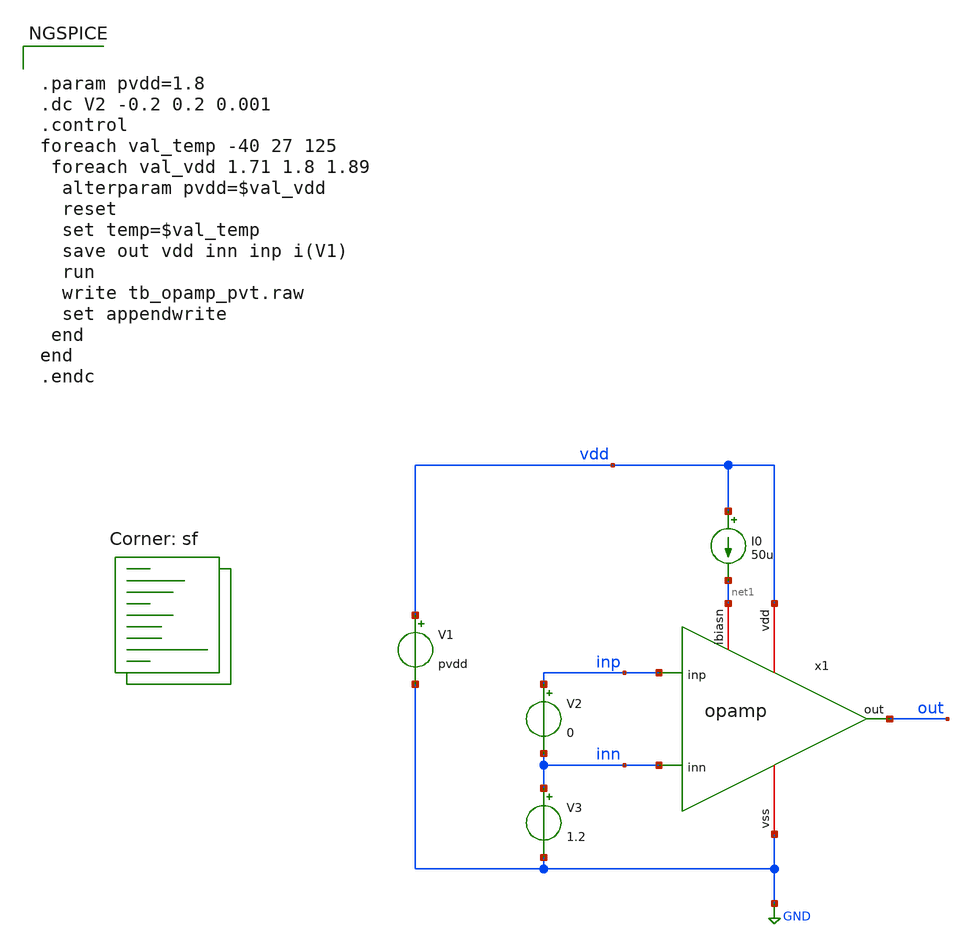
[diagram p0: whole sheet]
** sch_path: sky130A/HelloWorld/analog/schematic/tb_opamp_pvt.sch
**.subckt tb_opamp_pvt
x1 vdd out inp inn net1 GND opamp
V1 vdd GND pvdd
I0 vdd net1 50u
V2 inp inn 0
V3 inn GND 1.2
**** begin user architecture code


.param pvdd=1.8
.dc V2 -0.2 0.2 0.001
.control
foreach val_temp -40 27 125
 foreach val_vdd 1.71 1.8 1.89
  alterparam pvdd=$val_vdd
  reset
  set temp=$val_temp
  save out vdd inn inp i(V1)
  run
  write tb_opamp_pvt.raw
  set appendwrite
 end
end
.endc


.lib $::SKYWATER_MODELS/sky130.lib.spice sf
**** end user architecture code
**.ends

* expanding   symbol:  opamp.sym # of pins=6
** sym_path: sky130A/HelloWorld/xschem/opamp.sym
** sch_path: sky130A/HelloWorld/xschem/opamp.sch
.subckt opamp vdd out inp inn ibiasn vss
*.ipin inn
*.ipin inp
*.iopin vdd
*.iopin vss
*.iopin ibiasn
*.opin out
XM1 pbias inn tail vss sky130_fd_pr__nfet_01v8 L=1 W=40 nf=1 ad='int((nf+1)/2) * W/nf * 0.29' as='int((nf+2)/2) * W/nf * 0.29'
+ pd='2*int((nf+1)/2) * (W/nf + 0.29)' ps='2*int((nf+2)/2) * (W/nf + 0.29)' nrd='0.29 / W' nrs='0.29 / W'
+ sa=0 sb=0 sd=0 mult=1 m=1
XM2 outz inp tail vss sky130_fd_pr__nfet_01v8 L=1 W=40 nf=1 ad='int((nf+1)/2) * W/nf * 0.29' as='int((nf+2)/2) * W/nf * 0.29'
+ pd='2*int((nf+1)/2) * (W/nf + 0.29)' ps='2*int((nf+2)/2) * (W/nf + 0.29)' nrd='0.29 / W' nrs='0.29 / W'
+ sa=0 sb=0 sd=0 mult=1 m=1
XM3 pbias pbias vdd vdd sky130_fd_pr__pfet_01v8 L=0.5 W=20 nf=1 ad='int((nf+1)/2) * W/nf * 0.29' as='int((nf+2)/2) * W/nf * 0.29'
+ pd='2*int((nf+1)/2) * (W/nf + 0.29)' ps='2*int((nf+2)/2) * (W/nf + 0.29)' nrd='0.29 / W' nrs='0.29 / W'
+ sa=0 sb=0 sd=0 mult=1 m=1
XM4 outz pbias vdd vdd sky130_fd_pr__pfet_01v8 L=0.5 W=20 nf=1 ad='int((nf+1)/2) * W/nf * 0.29' as='int((nf+2)/2) * W/nf * 0.29'
+ pd='2*int((nf+1)/2) * (W/nf + 0.29)' ps='2*int((nf+2)/2) * (W/nf + 0.29)' nrd='0.29 / W' nrs='0.29 / W'
+ sa=0 sb=0 sd=0 mult=1 m=1
XM5 out outz vdd vdd sky130_fd_pr__pfet_01v8 L=0.5 W=20 nf=1 ad='int((nf+1)/2) * W/nf * 0.29' as='int((nf+2)/2) * W/nf * 0.29'
+ pd='2*int((nf+1)/2) * (W/nf + 0.29)' ps='2*int((nf+2)/2) * (W/nf + 0.29)' nrd='0.29 / W' nrs='0.29 / W'
+ sa=0 sb=0 sd=0 mult=1 m=1
XM6[1] tail ibiasn vss vss sky130_fd_pr__nfet_01v8 L=1 W=40 nf=1 ad='int((nf+1)/2) * W/nf * 0.29' as='int((nf+2)/2) * W/nf * 0.29'
+ pd='2*int((nf+1)/2) * (W/nf + 0.29)' ps='2*int((nf+2)/2) * (W/nf + 0.29)' nrd='0.29 / W' nrs='0.29 / W'
+ sa=0 sb=0 sd=0 mult=1 m=1
XM6[0] tail ibiasn vss vss sky130_fd_pr__nfet_01v8 L=1 W=40 nf=1 ad='int((nf+1)/2) * W/nf * 0.29' as='int((nf+2)/2) * W/nf * 0.29'
+ pd='2*int((nf+1)/2) * (W/nf + 0.29)' ps='2*int((nf+2)/2) * (W/nf + 0.29)' nrd='0.29 / W' nrs='0.29 / W'
+ sa=0 sb=0 sd=0 mult=1 m=1
XM7 out ibiasn vss vss sky130_fd_pr__nfet_01v8 L=1 W=40 nf=1 ad='int((nf+1)/2) * W/nf * 0.29' as='int((nf+2)/2) * W/nf * 0.29'
+ pd='2*int((nf+1)/2) * (W/nf + 0.29)' ps='2*int((nf+2)/2) * (W/nf + 0.29)' nrd='0.29 / W' nrs='0.29 / W'
+ sa=0 sb=0 sd=0 mult=1 m=1
XM8 ibiasn ibiasn vss vss sky130_fd_pr__nfet_01v8 L=1 W=40 nf=1 ad='int((nf+1)/2) * W/nf * 0.29' as='int((nf+2)/2) * W/nf * 0.29'
+ pd='2*int((nf+1)/2) * (W/nf + 0.29)' ps='2*int((nf+2)/2) * (W/nf + 0.29)' nrd='0.29 / W' nrs='0.29 / W'
+ sa=0 sb=0 sd=0 mult=1 m=1
.ends

.GLOBAL GND
.end
